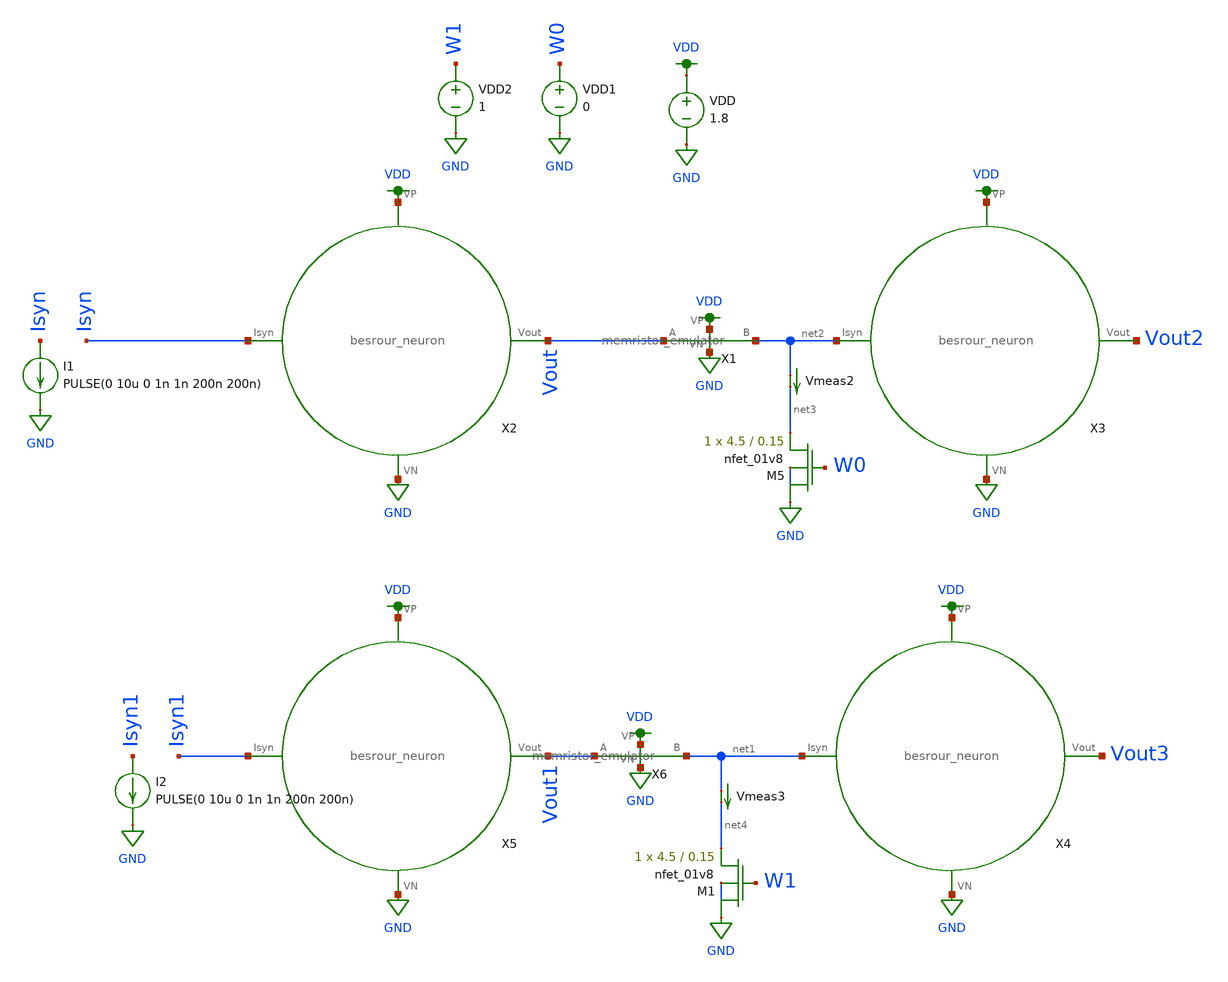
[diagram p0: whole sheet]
** sch_path: schematic/tran_besrour_mem.sch
**.subckt tran_besrour_mem
VDD VDD GND 1.8
VDD1 W0 GND 0
VDD2 W1 GND 1
I1 Isyn GND PULSE(0 10u 0 1n 1n 200n 200n)
I2 Isyn1 GND PULSE(0 10u 0 1n 1n 200n 200n)
Vmeas2 net2 net3 0
.save i(vmeas2)
XM5 GND W0 net3 GND sky130_fd_pr__nfet_01v8 L=0.15 W=4.5 nf=1 ad='int((nf+1)/2) * W/nf * 0.29' as='int((nf+2)/2) * W/nf * 0.29'
+ pd='2*int((nf+1)/2) * (W/nf + 0.29)' ps='2*int((nf+2)/2) * (W/nf + 0.29)' nrd='0.29 / W' nrs='0.29 / W'
+ sa=0 sb=0 sd=0 mult=1 m=1
Vmeas3 net1 net4 0
.save i(vmeas3)
XM1 GND W1 net4 GND sky130_fd_pr__nfet_01v8 L=0.15 W=4.5 nf=1 ad='int((nf+1)/2) * W/nf * 0.29' as='int((nf+2)/2) * W/nf * 0.29'
+ pd='2*int((nf+1)/2) * (W/nf + 0.29)' ps='2*int((nf+2)/2) * (W/nf + 0.29)' nrd='0.29 / W' nrs='0.29 / W'
+ sa=0 sb=0 sd=0 mult=1 m=1
X2 Isyn Vout VDD GND besrour_neuron
X3 net2 Vout2 VDD GND besrour_neuron
X4 net1 Vout3 VDD GND besrour_neuron
X5 Isyn1 Vout1 VDD GND besrour_neuron
X1 VDD GND net2 Vout memristor_emulator
X6 VDD GND net1 Vout1 memristor_emulator
**** begin user architecture code

.param W=1
.param L=0.15
.tran 0.1n 500n
.save all


.option wnflag=1
.param MC_SWITCH=0.0
.lib ~/skywater/skywater-pdk/libraries/sky130_fd_pr_ngspice/latest/models/sky130.lib.spice tt

**** end user architecture code
**.ends

* expanding   symbol:
*+  /home/madvlsi/Documents/second/neuromorphic_computing_final/schematic/besrour_neuron.sym # of pins=4
** sym_path: schematic/besrour_neuron.sym
** sch_path: schematic/besrour_neuron.sch
.subckt besrour_neuron Isyn Vout VP VN
*.iopin VP
*.iopin VN
*.iopin Isyn
*.opin Vout
XM1 VP Isyn Isyn VDD sky130_fd_pr__pfet_01v8 L={L} W={W} nf=1 ad='int((nf+1)/2) * W/nf * 0.29' as='int((nf+2)/2) * W/nf * 0.29'
+ pd='2*int((nf+1)/2) * (W/nf + 0.29)' ps='2*int((nf+2)/2) * (W/nf + 0.29)' nrd='0.29 / W' nrs='0.29 / W'
+ sa=0 sb=0 sd=0 mult=1 m=1
XM7 VN VPREOUT2 VMEMINT GND sky130_fd_pr__nfet_01v8 L={L} W={W} nf=1 ad='int((nf+1)/2) * W/nf * 0.29'
+ as='int((nf+2)/2) * W/nf * 0.29' pd='2*int((nf+1)/2) * (W/nf + 0.29)' ps='2*int((nf+2)/2) * (W/nf + 0.29)'
+ nrd='0.29 / W' nrs='0.29 / W' sa=0 sb=0 sd=0 mult=1 m=1
XM2 VMEMINT Isyn VP VDD sky130_fd_pr__pfet_01v8 L={L} W={W} nf=1 ad='int((nf+1)/2) * W/nf * 0.29' as='int((nf+2)/2) * W/nf * 0.29'
+ pd='2*int((nf+1)/2) * (W/nf + 0.29)' ps='2*int((nf+2)/2) * (W/nf + 0.29)' nrd='0.29 / W' nrs='0.29 / W'
+ sa=0 sb=0 sd=0 mult=1 m=1
XM3 VP net1 VMEMINT VDD sky130_fd_pr__pfet_01v8 L={L} W={W} nf=1 ad='int((nf+1)/2) * W/nf * 0.29' as='int((nf+2)/2) * W/nf * 0.29'
+ pd='2*int((nf+1)/2) * (W/nf + 0.29)' ps='2*int((nf+2)/2) * (W/nf + 0.29)' nrd='0.29 / W' nrs='0.29 / W'
+ sa=0 sb=0 sd=0 mult=1 m=1
XM4 net1 VMEMINT VP VDD sky130_fd_pr__pfet_01v8 L={L} W={W} nf=1 ad='int((nf+1)/2) * W/nf * 0.29' as='int((nf+2)/2) * W/nf * 0.29'
+ pd='2*int((nf+1)/2) * (W/nf + 0.29)' ps='2*int((nf+2)/2) * (W/nf + 0.29)' nrd='0.29 / W' nrs='0.29 / W'
+ sa=0 sb=0 sd=0 mult=1 m=1
XM5 VPREOUT2 net1 VP VDD sky130_fd_pr__pfet_01v8 L={L} W={W} nf=1 ad='int((nf+1)/2) * W/nf * 0.29' as='int((nf+2)/2) * W/nf * 0.29'
+ pd='2*int((nf+1)/2) * (W/nf + 0.29)' ps='2*int((nf+2)/2) * (W/nf + 0.29)' nrd='0.29 / W' nrs='0.29 / W'
+ sa=0 sb=0 sd=0 mult=1 m=1
XM6 net1 VMEMINT VN GND sky130_fd_pr__nfet_01v8 L={L} W={W} nf=1 ad='int((nf+1)/2) * W/nf * 0.29' as='int((nf+2)/2) * W/nf * 0.29'
+ pd='2*int((nf+1)/2) * (W/nf + 0.29)' ps='2*int((nf+2)/2) * (W/nf + 0.29)' nrd='0.29 / W' nrs='0.29 / W'
+ sa=0 sb=0 sd=0 mult=1 m=1
XM8 VPREOUT2 net1 VN GND sky130_fd_pr__nfet_01v8 L={L} W={W} nf=1 ad='int((nf+1)/2) * W/nf * 0.29' as='int((nf+2)/2) * W/nf * 0.29'
+ pd='2*int((nf+1)/2) * (W/nf + 0.29)' ps='2*int((nf+2)/2) * (W/nf + 0.29)' nrd='0.29 / W' nrs='0.29 / W'
+ sa=0 sb=0 sd=0 mult=1 m=1
C1 VMEMINT VN 340f m=1
C2 VPREOUT2 VN 340f m=1
XM9 VPREOUT VPREOUT2 VP VDD sky130_fd_pr__pfet_01v8 L={L} W={W} nf=1 ad='int((nf+1)/2) * W/nf * 0.29'
+ as='int((nf+2)/2) * W/nf * 0.29' pd='2*int((nf+1)/2) * (W/nf + 0.29)' ps='2*int((nf+2)/2) * (W/nf + 0.29)'
+ nrd='0.29 / W' nrs='0.29 / W' sa=0 sb=0 sd=0 mult=1 m=1
XM10 VPREOUT VPREOUT2 VN GND sky130_fd_pr__nfet_01v8 L={L} W={W} nf=1 ad='int((nf+1)/2) * W/nf * 0.29'
+ as='int((nf+2)/2) * W/nf * 0.29' pd='2*int((nf+1)/2) * (W/nf + 0.29)' ps='2*int((nf+2)/2) * (W/nf + 0.29)'
+ nrd='0.29 / W' nrs='0.29 / W' sa=0 sb=0 sd=0 mult=1 m=1
XM11 Vout VPREOUT VP VDD sky130_fd_pr__pfet_01v8 L={L} W={W} nf=1 ad='int((nf+1)/2) * W/nf * 0.29' as='int((nf+2)/2) * W/nf * 0.29'
+ pd='2*int((nf+1)/2) * (W/nf + 0.29)' ps='2*int((nf+2)/2) * (W/nf + 0.29)' nrd='0.29 / W' nrs='0.29 / W'
+ sa=0 sb=0 sd=0 mult=1 m=1
XM12 Vout VPREOUT VN GND sky130_fd_pr__nfet_01v8 L={L} W={W} nf=1 ad='int((nf+1)/2) * W/nf * 0.29' as='int((nf+2)/2) * W/nf * 0.29'
+ pd='2*int((nf+1)/2) * (W/nf + 0.29)' ps='2*int((nf+2)/2) * (W/nf + 0.29)' nrd='0.29 / W' nrs='0.29 / W'
+ sa=0 sb=0 sd=0 mult=1 m=1
.ends


* expanding   symbol:
*+  /home/madvlsi/Documents/second/neuromorphic_computing_final/schematic/memristor_emulator.sym # of pins=4
** sym_path: schematic/memristor_emulator.sym
** sch_path: schematic/memristor_emulator.sch
.subckt memristor_emulator VP VN B A
*.ipin A
*.iopin VN
*.iopin VP
*.opin B
XM1 B net1 A B sky130_fd_pr__pfet_01v8 L=0.15 W=12 nf=1 ad='int((nf+1)/2) * W/nf * 0.29' as='int((nf+2)/2) * W/nf * 0.29'
+ pd='2*int((nf+1)/2) * (W/nf + 0.29)' ps='2*int((nf+2)/2) * (W/nf + 0.29)' nrd='0.29 / W' nrs='0.29 / W'
+ sa=0 sb=0 sd=0 mult=1 m=1
XM2 VP A net1 VP sky130_fd_pr__pfet_01v8 L=2 W=3 nf=1 ad='int((nf+1)/2) * W/nf * 0.29' as='int((nf+2)/2) * W/nf * 0.29'
+ pd='2*int((nf+1)/2) * (W/nf + 0.29)' ps='2*int((nf+2)/2) * (W/nf + 0.29)' nrd='0.29 / W' nrs='0.29 / W'
+ sa=0 sb=0 sd=0 mult=1 m=1
XM3 VN net1 VN VN sky130_fd_pr__nfet_01v8 L=4 W=3 nf=1 ad='int((nf+1)/2) * W/nf * 0.29' as='int((nf+2)/2) * W/nf * 0.29'
+ pd='2*int((nf+1)/2) * (W/nf + 0.29)' ps='2*int((nf+2)/2) * (W/nf + 0.29)' nrd='0.29 / W' nrs='0.29 / W'
+ sa=0 sb=0 sd=0 mult=1 m=1
XM4 VN B net1 VN sky130_fd_pr__nfet_01v8 L=3 W=2 nf=1 ad='int((nf+1)/2) * W/nf * 0.29' as='int((nf+2)/2) * W/nf * 0.29'
+ pd='2*int((nf+1)/2) * (W/nf + 0.29)' ps='2*int((nf+2)/2) * (W/nf + 0.29)' nrd='0.29 / W' nrs='0.29 / W'
+ sa=0 sb=0 sd=0 mult=1 m=1
.ends

.GLOBAL VDD
.GLOBAL GND
.end
